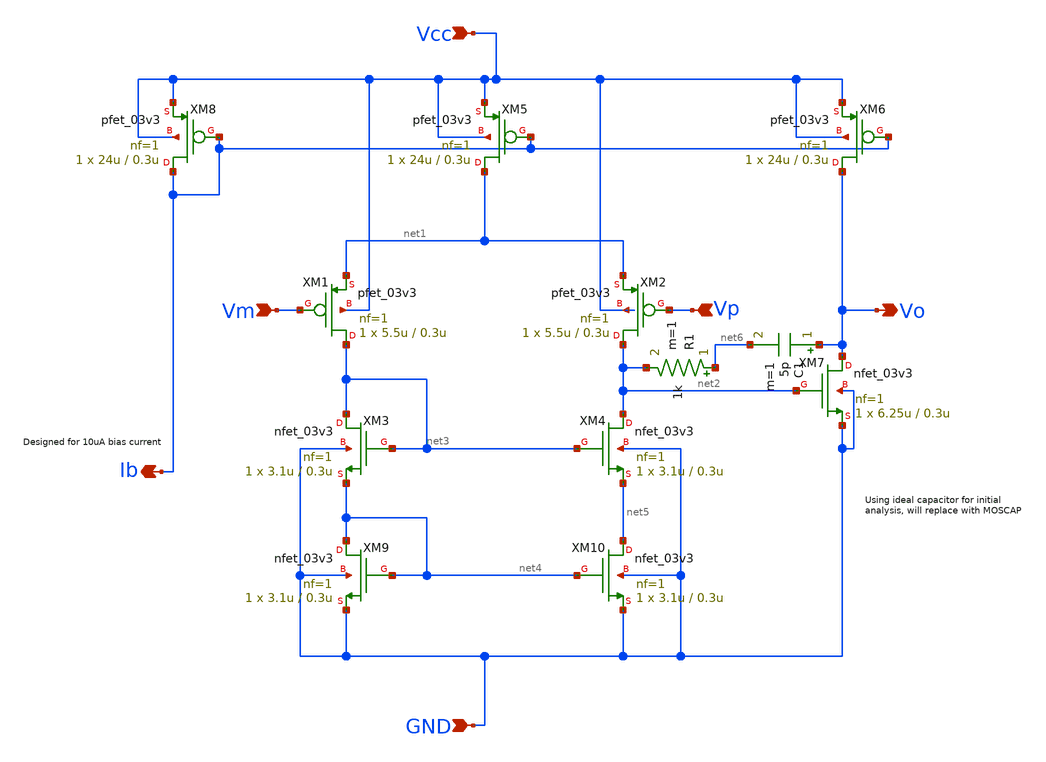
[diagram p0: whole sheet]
** sch_path: op_amp_dir_comp.sch
**.subckt op_amp_dir_comp Vm Vp Vcc GND Ib Vo
*.ipin Vm
*.ipin Vp
*.ipin Vcc
*.ipin GND
*.opin Ib
*.opin Vo
XM3 net3 net3 net4 GND nfet_03v3 L=0.3u W=3.1u nf=1 ad='int((nf+1)/2) * W/nf * 0.18u' as='int((nf+2)/2) * W/nf * 0.18u'
+ pd='2*int((nf+1)/2) * (W/nf + 0.18u)' ps='2*int((nf+2)/2) * (W/nf + 0.18u)' nrd='0.18u / W' nrs='0.18u / W'
+ sa=0 sb=0 sd=0 m=1 par=1
XM1 net3 Vm net1 Vcc pfet_03v3 L=0.3u W=5.5u nf=1 ad='int((nf+1)/2) * W/nf * 0.18u' as='int((nf+2)/2) * W/nf * 0.18u'
+ pd='2*int((nf+1)/2) * (W/nf + 0.18u)' ps='2*int((nf+2)/2) * (W/nf + 0.18u)' nrd='0.18u / W' nrs='0.18u / W'
+ sa=0 sb=0 sd=0 m=1 par=1
XM4 net2 net3 net5 GND nfet_03v3 L=0.3u W=3.1u nf=1 ad='int((nf+1)/2) * W/nf * 0.18u' as='int((nf+2)/2) * W/nf * 0.18u'
+ pd='2*int((nf+1)/2) * (W/nf + 0.18u)' ps='2*int((nf+2)/2) * (W/nf + 0.18u)' nrd='0.18u / W' nrs='0.18u / W'
+ sa=0 sb=0 sd=0 m=1 par=1
XM2 net2 Vp net1 Vcc pfet_03v3 L=0.3u W=5.5u nf=1 ad='int((nf+1)/2) * W/nf * 0.18u' as='int((nf+2)/2) * W/nf * 0.18u'
+ pd='2*int((nf+1)/2) * (W/nf + 0.18u)' ps='2*int((nf+2)/2) * (W/nf + 0.18u)' nrd='0.18u / W' nrs='0.18u / W'
+ sa=0 sb=0 sd=0 m=1 par=1
XM5 net1 Ib Vcc Vcc pfet_03v3 L=0.3u W=24u nf=1 ad='int((nf+1)/2) * W/nf * 0.18u' as='int((nf+2)/2) * W/nf * 0.18u'
+ pd='2*int((nf+1)/2) * (W/nf + 0.18u)' ps='2*int((nf+2)/2) * (W/nf + 0.18u)' nrd='0.18u / W' nrs='0.18u / W'
+ sa=0 sb=0 sd=0 m=1 par=1
XM6 Vo Ib Vcc Vcc pfet_03v3 L=0.3u W=24u nf=1 ad='int((nf+1)/2) * W/nf * 0.18u' as='int((nf+2)/2) * W/nf * 0.18u'
+ pd='2*int((nf+1)/2) * (W/nf + 0.18u)' ps='2*int((nf+2)/2) * (W/nf + 0.18u)' nrd='0.18u / W' nrs='0.18u / W'
+ sa=0 sb=0 sd=0 m=1 par=1
XM8 Ib Ib Vcc Vcc pfet_03v3 L=0.3u W=24u nf=1 ad='int((nf+1)/2) * W/nf * 0.18u' as='int((nf+2)/2) * W/nf * 0.18u'
+ pd='2*int((nf+1)/2) * (W/nf + 0.18u)' ps='2*int((nf+2)/2) * (W/nf + 0.18u)' nrd='0.18u / W' nrs='0.18u / W'
+ sa=0 sb=0 sd=0 m=1 par=1
XM7 Vo net2 GND GND nfet_03v3 L=0.3u W=6.25u nf=1 ad='int((nf+1)/2) * W/nf * 0.18u' as='int((nf+2)/2) * W/nf * 0.18u'
+ pd='2*int((nf+1)/2) * (W/nf + 0.18u)' ps='2*int((nf+2)/2) * (W/nf + 0.18u)' nrd='0.18u / W' nrs='0.18u / W'
+ sa=0 sb=0 sd=0 m=1 par=1
XM9 net4 net4 GND GND nfet_03v3 L=0.3u W=3.1u nf=1 ad='int((nf+1)/2) * W/nf * 0.18u' as='int((nf+2)/2) * W/nf * 0.18u'
+ pd='2*int((nf+1)/2) * (W/nf + 0.18u)' ps='2*int((nf+2)/2) * (W/nf + 0.18u)' nrd='0.18u / W' nrs='0.18u / W'
+ sa=0 sb=0 sd=0 m=1 par=1
XM10 net5 net4 GND GND nfet_03v3 L=0.3u W=3.1u nf=1 ad='int((nf+1)/2) * W/nf * 0.18u' as='int((nf+2)/2) * W/nf * 0.18u'
+ pd='2*int((nf+1)/2) * (W/nf + 0.18u)' ps='2*int((nf+2)/2) * (W/nf + 0.18u)' nrd='0.18u / W' nrs='0.18u / W'
+ sa=0 sb=0 sd=0 m=1 par=1
C1 Vo net6 5p m=1
R1 net6 net2 1k m=1
**.ends
.end
